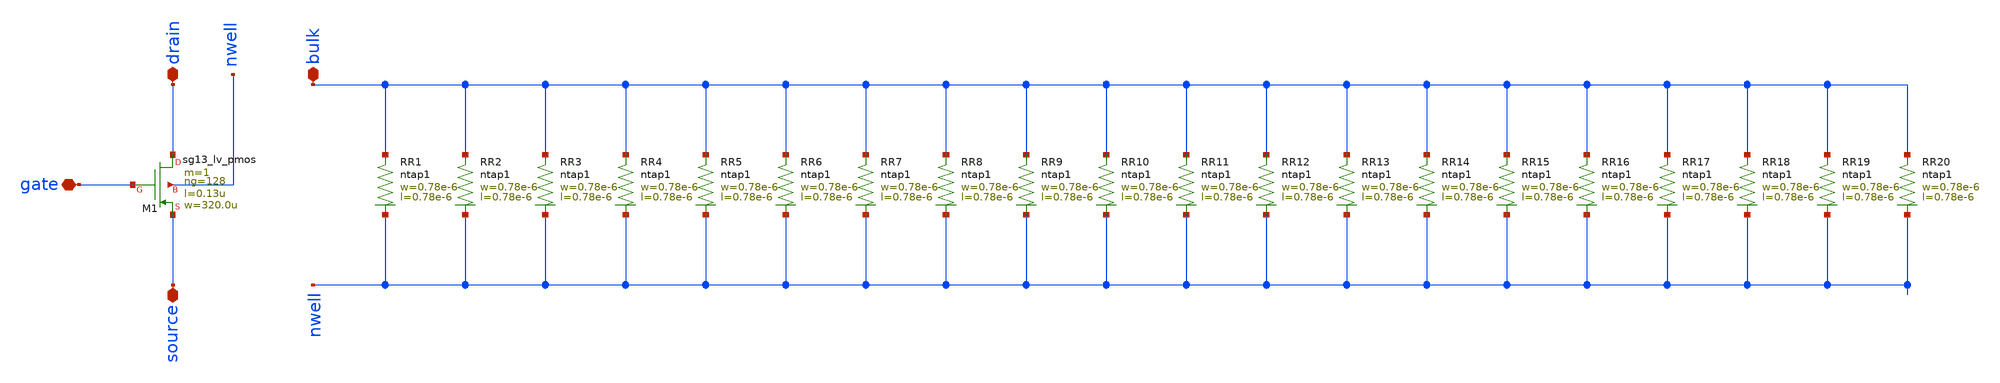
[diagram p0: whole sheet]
** sch_path: ts_pr_May2024/design_data/xschem/pmos128.sch
**.subckt pmos128 gate drain source bulk
*.iopin gate
*.iopin drain
*.iopin source
*.iopin bulk
XM1 drain gate source nwell sg13_lv_pmos w=320.0u l=0.13u ng=128 m=1 mm_ok=1
XR1 bulk nwell ntap1 R=262.8 w=0.78e-6 l=0.78e-6
XR2 bulk nwell ntap1 R=262.8 w=0.78e-6 l=0.78e-6
XR3 bulk nwell ntap1 R=262.8 w=0.78e-6 l=0.78e-6
XR4 bulk nwell ntap1 R=262.8 w=0.78e-6 l=0.78e-6
XR5 bulk nwell ntap1 R=262.8 w=0.78e-6 l=0.78e-6
XR6 bulk nwell ntap1 R=262.8 w=0.78e-6 l=0.78e-6
XR7 bulk nwell ntap1 R=262.8 w=0.78e-6 l=0.78e-6
XR8 bulk nwell ntap1 R=262.8 w=0.78e-6 l=0.78e-6
XR9 bulk nwell ntap1 R=262.8 w=0.78e-6 l=0.78e-6
XR10 bulk nwell ntap1 R=262.8 w=0.78e-6 l=0.78e-6
XR11 bulk nwell ntap1 R=262.8 w=0.78e-6 l=0.78e-6
XR12 bulk nwell ntap1 R=262.8 w=0.78e-6 l=0.78e-6
XR13 bulk nwell ntap1 R=262.8 w=0.78e-6 l=0.78e-6
XR14 bulk nwell ntap1 R=262.8 w=0.78e-6 l=0.78e-6
XR15 bulk nwell ntap1 R=262.8 w=0.78e-6 l=0.78e-6
XR16 bulk nwell ntap1 R=262.8 w=0.78e-6 l=0.78e-6
XR17 bulk nwell ntap1 R=262.8 w=0.78e-6 l=0.78e-6
XR18 bulk nwell ntap1 R=262.8 w=0.78e-6 l=0.78e-6
XR19 bulk nwell ntap1 R=262.8 w=0.78e-6 l=0.78e-6
XR20 bulk nwell ntap1 R=262.8 w=0.78e-6 l=0.78e-6
**.ends
.end
